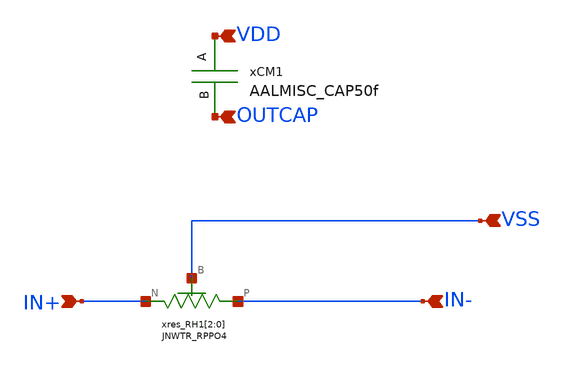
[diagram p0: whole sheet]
** sch_path: design/JNW_BKLE_SKY130A/RC_EXT.sch
**.subckt RC_EXT VSS IN- IN+ VDD OUTCAP
*.ipin VSS
*.ipin IN-
*.ipin IN+
*.ipin VDD
*.ipin OUTCAP
xres_RH1[2] IN+ IN- VSS JNWTR_RPPO4 xoffset=0 yoffset=0 angle=0
xres_RH1[1] IN+ IN- VSS JNWTR_RPPO4 xoffset=0 yoffset=0 angle=0
xres_RH1[0] IN+ IN- VSS JNWTR_RPPO4 xoffset=0 yoffset=0 angle=0
xCM1 VDD OUTCAP AALMISC_CAP50f
**.ends

* expanding   symbol:  JNW_TR_SKY130A/JNWTR_RPPO4.sym # of pins=3
** sym_path: JNW_TR_SKY130A/JNWTR_RPPO4.sym
** sch_path: JNW_TR_SKY130A/JNWTR_RPPO4.sch
.subckt JNWTR_RPPO4 N P B  xoffset=0 yoffset=0 angle=0
*.iopin P
*.iopin N
*.iopin B
XXA1 N P B JNWTR_RES4
.ends


* expanding   symbol:  AAL_MISC_SKY130A/AALMISC_CAP50f.sym # of pins=2
** sym_path: design/AAL_MISC_SKY130A/AALMISC_CAP50f.sym
** sch_path: design/AAL_MISC_SKY130A/AALMISC_CAP50f.sch
.subckt AALMISC_CAP50f A B
*.iopin A
*.iopin B
XC1 A B sky130_fd_pr__cap_mim_m3_2 W=5 L=5 MF=1 m=1
.ends


* expanding   symbol:  JNW_TR_SKY130A/JNWTR_RES4.sym # of pins=3
** sym_path: JNW_TR_SKY130A/JNWTR_RES4.sym
** sch_path: JNW_TR_SKY130A/JNWTR_RES4.sch
.subckt JNWTR_RES4 N P B
*.iopin N
*.iopin P
*.iopin B
XR1_0 INT_0 N B sky130_fd_pr__res_high_po W=0.36 L=7.2 mult=1 m=1
XR1_1 INT_1 INT_0 B sky130_fd_pr__res_high_po W=0.36 L=7.2 mult=1 m=1
XR1_2 INT_2 INT_1 B sky130_fd_pr__res_high_po W=0.36 L=7.2 mult=1 m=1
XR1_3 P INT_2 B sky130_fd_pr__res_high_po W=0.36 L=7.2 mult=1 m=1
.ends

.end
